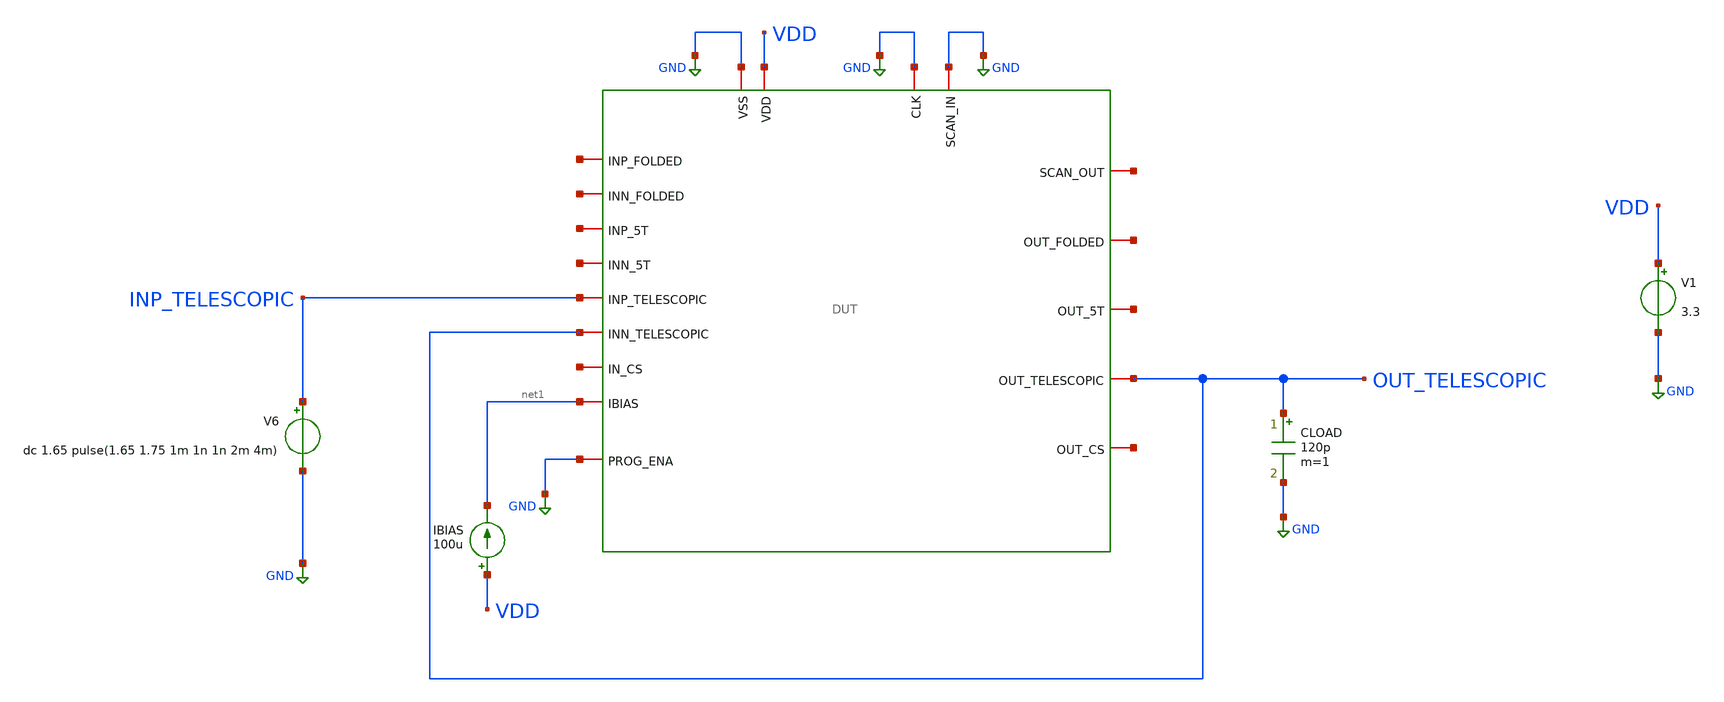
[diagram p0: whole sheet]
** sch_path: designs/libs/pex/tele/step_response/default_step_tele.sch
**.subckt default_step_tele
V1 VDD GND 3.3
CLOAD OUT_TELESCOPIC GND 120p m=1
V6 INP_TELESCOPIC GND dc 1.65 pulse(1.65 1.75 1m 1n 1n 2m 4m)
IBIAS VDD net1 100u
x1 GND net2 GND GND VDD net3 net4 net5 net1 net6 net7 net8 INP_TELESCOPIC OUT_TELESCOPIC net9 net10
+ OUT_TELESCOPIC GND DUT
**** begin user architecture code

.include $::180MCU_MODELS/design.ngspice
.lib $::180MCU_MODELS/sm141064.ngspice typical



.include /foss/designs/libs/pex/DUT.spice
.control
tran 1u 5m

plot v(out_telescopic) v(inp_telescopic)

meas tran v_before find v(out_telescopic) at=0.99m
meas tran v_after find v(out_telescopic) at=2.5m

let delta = v_after - v_before
let t20_val = v_before + 0.2 * delta
let t80_val = v_before + 0.8 * delta

meas tran t_20 when v(out_telescopic) = t20_val rise = 1
meas tran t_80 when v(out_telescopic) = t80_val rise = 1
let sr_rise = delta / (t_80 - t_20)
print sr_rise

meas tran t_20f when v(out_telescopic) = t80_val fall = 1
meas tran t_80f when v(out_telescopic) = t20_val fall = 1
let sr_fall = delta / (t_80f - t_20f)
print sr_fall

meas tran vpeak max v(out_telescopic) from=1m to=3m
let overshoot = (vpeak - v_after) / delta * 100
print overshoot

meas tran t_settle when v(out_telescopic) = v_after td = 1m rise = 1
let settling = t_settle - 1m
print settling

print v_before v_after delta
.endc


**** end user architecture code
**.ends
.GLOBAL GND
.end
